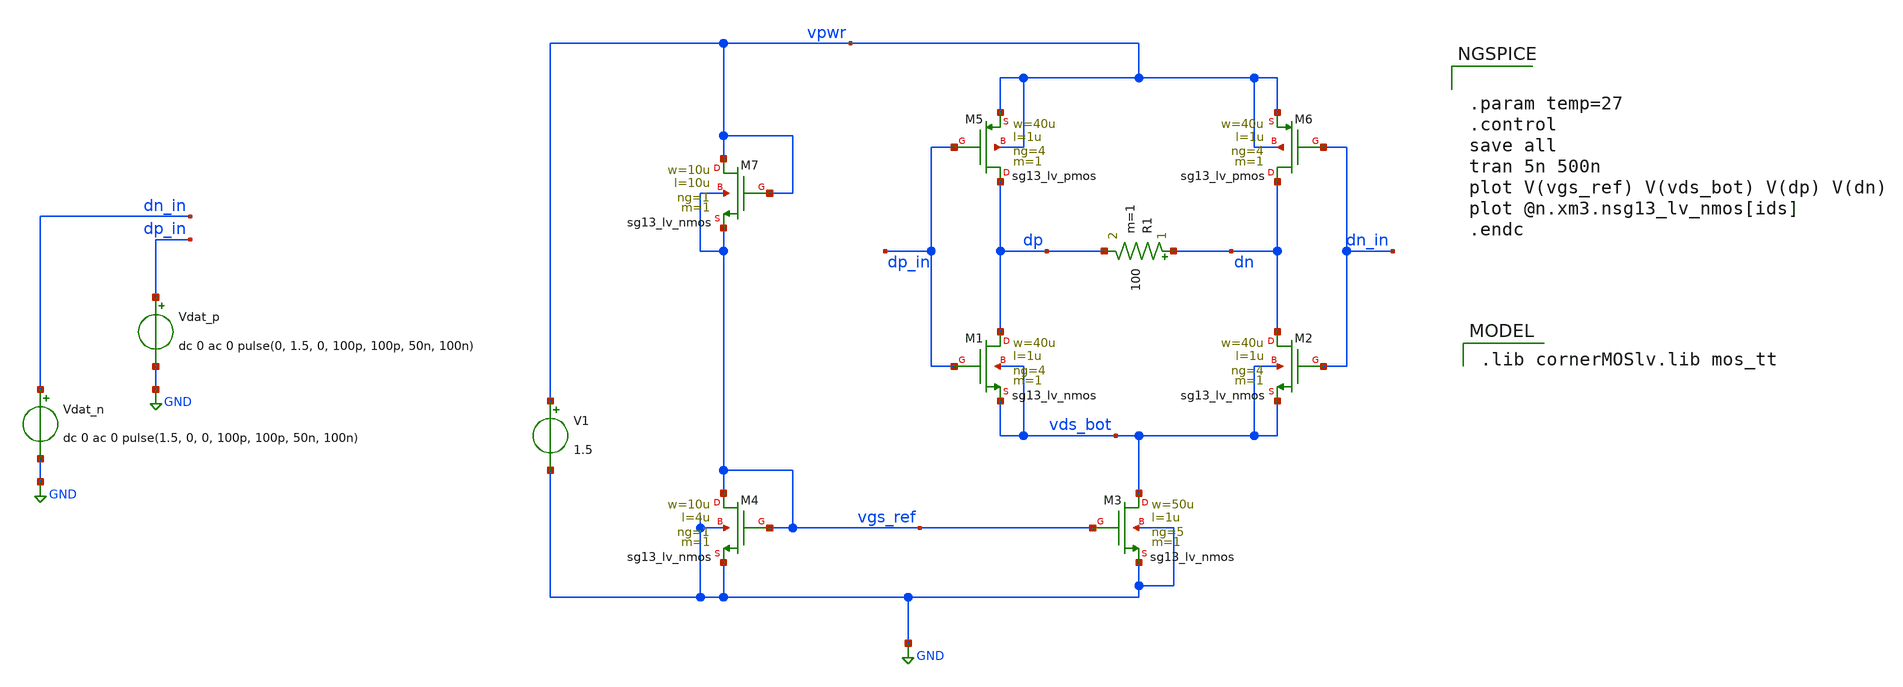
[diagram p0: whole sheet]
** sch_path: xschem/lvds_full_test.sch
**.subckt lvds_full_test
XM1 dp dp_in vds_bot vds_bot sg13_lv_nmos w=40u l=1u ng=4 m=1 mm_ok=1
XM2 dn dn_in vds_bot vds_bot sg13_lv_nmos w=40u l=1u ng=4 m=1 mm_ok=1
XM5 dp dp_in vpwr vpwr sg13_lv_pmos w=40u l=1u ng=4 m=1 mm_ok=1
XM6 dn dn_in vpwr vpwr sg13_lv_pmos w=40u l=1u ng=4 m=1 mm_ok=1
XM3 vds_bot vgs_ref GND GND sg13_lv_nmos w=50u l=1u ng=5 m=1 mm_ok=1
XM4 vgs_ref vgs_ref GND GND sg13_lv_nmos w=10u l=4u ng=1 m=1 mm_ok=1
V1 vpwr GND 1.5
Vdat_p dp_in GND dc 0 ac 0 pulse(0, 1.5, 0, 100p, 100p, 50n, 100n)
Vdat_n dn_in GND dc 0 ac 0 pulse(1.5, 0, 0, 100p, 100p, 50n, 100n)
R1 dn dp 100 m=1
XM7 vpwr vpwr vgs_ref vgs_ref sg13_lv_nmos w=10u l=10u ng=1 m=1 mm_ok=1
**** begin user architecture code
 .lib cornerMOSlv.lib mos_tt



.param temp=27
.control
save all
tran 5n 500n
plot V(vgs_ref) V(vds_bot) V(dp) V(dn)
plot @n.xm3.nsg13_lv_nmos[ids]
.endc


**** end user architecture code
**.ends
.GLOBAL GND
.end
